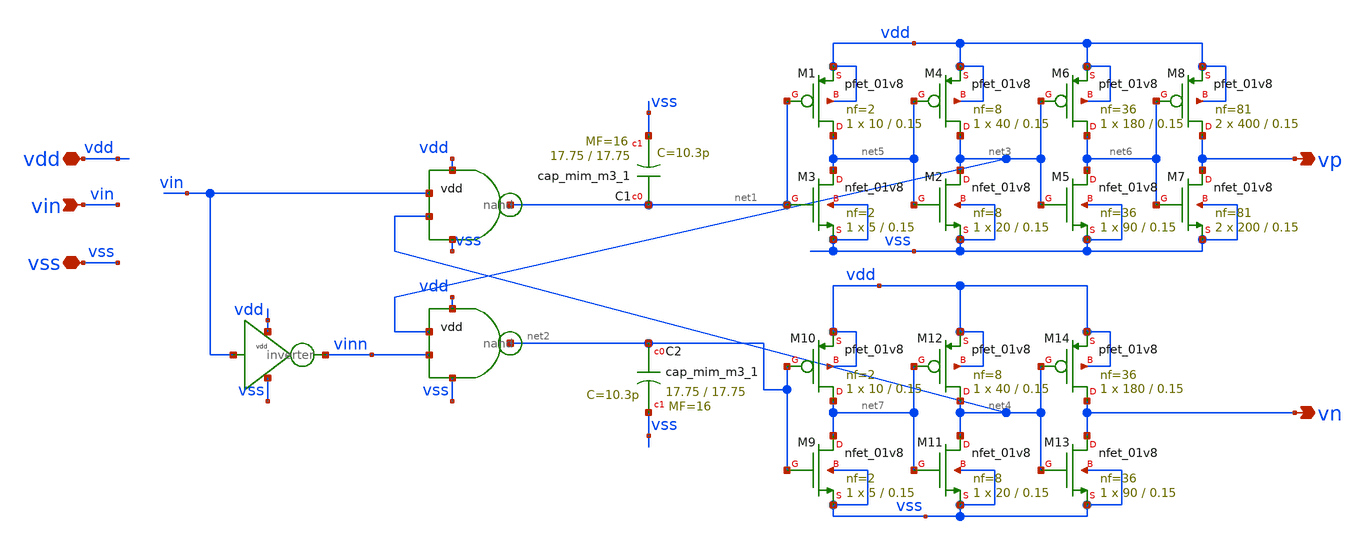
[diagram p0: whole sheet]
** sch_path: xschem/src/dead_time/dead_time.sch
**.subckt dead_time vin vdd vp vss vn
*.ipin vin
*.iopin vdd
*.opin vp
*.iopin vss
*.opin vn
x1 vdd vin vinn vss inverter
x2 vdd net1 vin net4 vss nand
x3 vdd net2 net3 vinn vss nand
XC1 net1 vss sky130_fd_pr__cap_mim_m3_1 W=17.75 L=17.75 MF=16 m=16
XM3 net5 net1 vss vss sky130_fd_pr__nfet_01v8 L=0.15 W=5 nf=2 ad='int((nf+1)/2) * W/nf * 0.29' as='int((nf+2)/2) * W/nf * 0.29'
+ pd='2*int((nf+1)/2) * (W/nf + 0.29)' ps='2*int((nf+2)/2) * (W/nf + 0.29)' nrd='0.29 / W' nrs='0.29 / W'
+ sa=0 sb=0 sd=0 mult=1 m=1
XM1 net5 net1 vdd vdd sky130_fd_pr__pfet_01v8 L=0.15 W=10 nf=2 ad='int((nf+1)/2) * W/nf * 0.29' as='int((nf+2)/2) * W/nf * 0.29'
+ pd='2*int((nf+1)/2) * (W/nf + 0.29)' ps='2*int((nf+2)/2) * (W/nf + 0.29)' nrd='0.29 / W' nrs='0.29 / W'
+ sa=0 sb=0 sd=0 mult=1 m=1
XM2 net3 net5 vss vss sky130_fd_pr__nfet_01v8 L=0.15 W=20 nf=8 ad='int((nf+1)/2) * W/nf * 0.29' as='int((nf+2)/2) * W/nf * 0.29'
+ pd='2*int((nf+1)/2) * (W/nf + 0.29)' ps='2*int((nf+2)/2) * (W/nf + 0.29)' nrd='0.29 / W' nrs='0.29 / W'
+ sa=0 sb=0 sd=0 mult=1 m=1
XM4 net3 net5 vdd vdd sky130_fd_pr__pfet_01v8 L=0.15 W=40 nf=8 ad='int((nf+1)/2) * W/nf * 0.29' as='int((nf+2)/2) * W/nf * 0.29'
+ pd='2*int((nf+1)/2) * (W/nf + 0.29)' ps='2*int((nf+2)/2) * (W/nf + 0.29)' nrd='0.29 / W' nrs='0.29 / W'
+ sa=0 sb=0 sd=0 mult=1 m=1
XM5 net6 net3 vss vss sky130_fd_pr__nfet_01v8 L=0.15 W=90 nf=36 ad='int((nf+1)/2) * W/nf * 0.29' as='int((nf+2)/2) * W/nf * 0.29'
+ pd='2*int((nf+1)/2) * (W/nf + 0.29)' ps='2*int((nf+2)/2) * (W/nf + 0.29)' nrd='0.29 / W' nrs='0.29 / W'
+ sa=0 sb=0 sd=0 mult=1 m=1
XM6 net6 net3 vdd vdd sky130_fd_pr__pfet_01v8 L=0.15 W=180 nf=36 ad='int((nf+1)/2) * W/nf * 0.29' as='int((nf+2)/2) * W/nf * 0.29'
+ pd='2*int((nf+1)/2) * (W/nf + 0.29)' ps='2*int((nf+2)/2) * (W/nf + 0.29)' nrd='0.29 / W' nrs='0.29 / W'
+ sa=0 sb=0 sd=0 mult=1 m=1
XM7 vp net6 vss vss sky130_fd_pr__nfet_01v8 L=0.15 W=200 nf=81 ad='int((nf+1)/2) * W/nf * 0.29' as='int((nf+2)/2) * W/nf * 0.29'
+ pd='2*int((nf+1)/2) * (W/nf + 0.29)' ps='2*int((nf+2)/2) * (W/nf + 0.29)' nrd='0.29 / W' nrs='0.29 / W'
+ sa=0 sb=0 sd=0 mult=2 m=2
XM8 vp net6 vdd vdd sky130_fd_pr__pfet_01v8 L=0.15 W=400 nf=81 ad='int((nf+1)/2) * W/nf * 0.29' as='int((nf+2)/2) * W/nf * 0.29'
+ pd='2*int((nf+1)/2) * (W/nf + 0.29)' ps='2*int((nf+2)/2) * (W/nf + 0.29)' nrd='0.29 / W' nrs='0.29 / W'
+ sa=0 sb=0 sd=0 mult=2 m=2
XM9 net7 net2 vss vss sky130_fd_pr__nfet_01v8 L=0.15 W=5 nf=2 ad='int((nf+1)/2) * W/nf * 0.29' as='int((nf+2)/2) * W/nf * 0.29'
+ pd='2*int((nf+1)/2) * (W/nf + 0.29)' ps='2*int((nf+2)/2) * (W/nf + 0.29)' nrd='0.29 / W' nrs='0.29 / W'
+ sa=0 sb=0 sd=0 mult=1 m=1
XM10 net7 net2 vdd vdd sky130_fd_pr__pfet_01v8 L=0.15 W=10 nf=2 ad='int((nf+1)/2) * W/nf * 0.29' as='int((nf+2)/2) * W/nf * 0.29'
+ pd='2*int((nf+1)/2) * (W/nf + 0.29)' ps='2*int((nf+2)/2) * (W/nf + 0.29)' nrd='0.29 / W' nrs='0.29 / W'
+ sa=0 sb=0 sd=0 mult=1 m=1
XM11 net4 net7 vss vss sky130_fd_pr__nfet_01v8 L=0.15 W=20 nf=8 ad='int((nf+1)/2) * W/nf * 0.29' as='int((nf+2)/2) * W/nf * 0.29'
+ pd='2*int((nf+1)/2) * (W/nf + 0.29)' ps='2*int((nf+2)/2) * (W/nf + 0.29)' nrd='0.29 / W' nrs='0.29 / W'
+ sa=0 sb=0 sd=0 mult=1 m=1
XM12 net4 net7 vdd vdd sky130_fd_pr__pfet_01v8 L=0.15 W=40 nf=8 ad='int((nf+1)/2) * W/nf * 0.29' as='int((nf+2)/2) * W/nf * 0.29'
+ pd='2*int((nf+1)/2) * (W/nf + 0.29)' ps='2*int((nf+2)/2) * (W/nf + 0.29)' nrd='0.29 / W' nrs='0.29 / W'
+ sa=0 sb=0 sd=0 mult=1 m=1
XM13 vn net4 vss vss sky130_fd_pr__nfet_01v8 L=0.15 W=90 nf=36 ad='int((nf+1)/2) * W/nf * 0.29' as='int((nf+2)/2) * W/nf * 0.29'
+ pd='2*int((nf+1)/2) * (W/nf + 0.29)' ps='2*int((nf+2)/2) * (W/nf + 0.29)' nrd='0.29 / W' nrs='0.29 / W'
+ sa=0 sb=0 sd=0 mult=1 m=1
XM14 vn net4 vdd vdd sky130_fd_pr__pfet_01v8 L=0.15 W=180 nf=36 ad='int((nf+1)/2) * W/nf * 0.29' as='int((nf+2)/2) * W/nf * 0.29'
+ pd='2*int((nf+1)/2) * (W/nf + 0.29)' ps='2*int((nf+2)/2) * (W/nf + 0.29)' nrd='0.29 / W' nrs='0.29 / W'
+ sa=0 sb=0 sd=0 mult=1 m=1
XC2 net2 vss sky130_fd_pr__cap_mim_m3_1 W=17.75 L=17.75 MF=16 m=16
**.ends

* expanding   symbol:  src/inverter/inverter.sym # of pins=4
** sym_path: xschem/src/inverter/inverter.sym
** sch_path: xschem/src/inverter/inverter.sch
.subckt inverter vdd A B vss
*.iopin vdd
*.iopin vss
*.ipin A
*.opin B
XM3 B A vss vss sky130_fd_pr__nfet_01v8 L=0.15 W=1 nf=1 ad='int((nf+1)/2) * W/nf * 0.29' as='int((nf+2)/2) * W/nf * 0.29'
+ pd='2*int((nf+1)/2) * (W/nf + 0.29)' ps='2*int((nf+2)/2) * (W/nf + 0.29)' nrd='0.29 / W' nrs='0.29 / W'
+ sa=0 sb=0 sd=0 mult=1 m=1
XM1 B A vdd vdd sky130_fd_pr__pfet_01v8 L=0.15 W=2 nf=1 ad='int((nf+1)/2) * W/nf * 0.29' as='int((nf+2)/2) * W/nf * 0.29'
+ pd='2*int((nf+1)/2) * (W/nf + 0.29)' ps='2*int((nf+2)/2) * (W/nf + 0.29)' nrd='0.29 / W' nrs='0.29 / W'
+ sa=0 sb=0 sd=0 mult=1 m=1
.ends


* expanding   symbol:  src/nand/nand.sym # of pins=5
** sym_path: xschem/src/nand/nand.sym
** sch_path: xschem/src/nand/nand.sch
.subckt nand vdd out A B vss
*.ipin A
*.ipin B
*.opin out
*.iopin vdd
*.iopin vss
XM1 out A net1 vss sky130_fd_pr__nfet_01v8 L=0.15 W=2 nf=1 ad='int((nf+1)/2) * W/nf * 0.29' as='int((nf+2)/2) * W/nf * 0.29'
+ pd='2*int((nf+1)/2) * (W/nf + 0.29)' ps='2*int((nf+2)/2) * (W/nf + 0.29)' nrd='0.29 / W' nrs='0.29 / W'
+ sa=0 sb=0 sd=0 mult=1 m=1
XM2 out A vdd vdd sky130_fd_pr__pfet_01v8 L=0.15 W=2 nf=1 ad='int((nf+1)/2) * W/nf * 0.29' as='int((nf+2)/2) * W/nf * 0.29'
+ pd='2*int((nf+1)/2) * (W/nf + 0.29)' ps='2*int((nf+2)/2) * (W/nf + 0.29)' nrd='0.29 / W' nrs='0.29 / W'
+ sa=0 sb=0 sd=0 mult=1 m=1
XM3 net1 B vss vss sky130_fd_pr__nfet_01v8 L=0.15 W=2 nf=1 ad='int((nf+1)/2) * W/nf * 0.29' as='int((nf+2)/2) * W/nf * 0.29'
+ pd='2*int((nf+1)/2) * (W/nf + 0.29)' ps='2*int((nf+2)/2) * (W/nf + 0.29)' nrd='0.29 / W' nrs='0.29 / W'
+ sa=0 sb=0 sd=0 mult=1 m=1
XM4 out B vdd vdd sky130_fd_pr__pfet_01v8 L=0.15 W=2 nf=1 ad='int((nf+1)/2) * W/nf * 0.29' as='int((nf+2)/2) * W/nf * 0.29'
+ pd='2*int((nf+1)/2) * (W/nf + 0.29)' ps='2*int((nf+2)/2) * (W/nf + 0.29)' nrd='0.29 / W' nrs='0.29 / W'
+ sa=0 sb=0 sd=0 mult=1 m=1
.ends

.end
